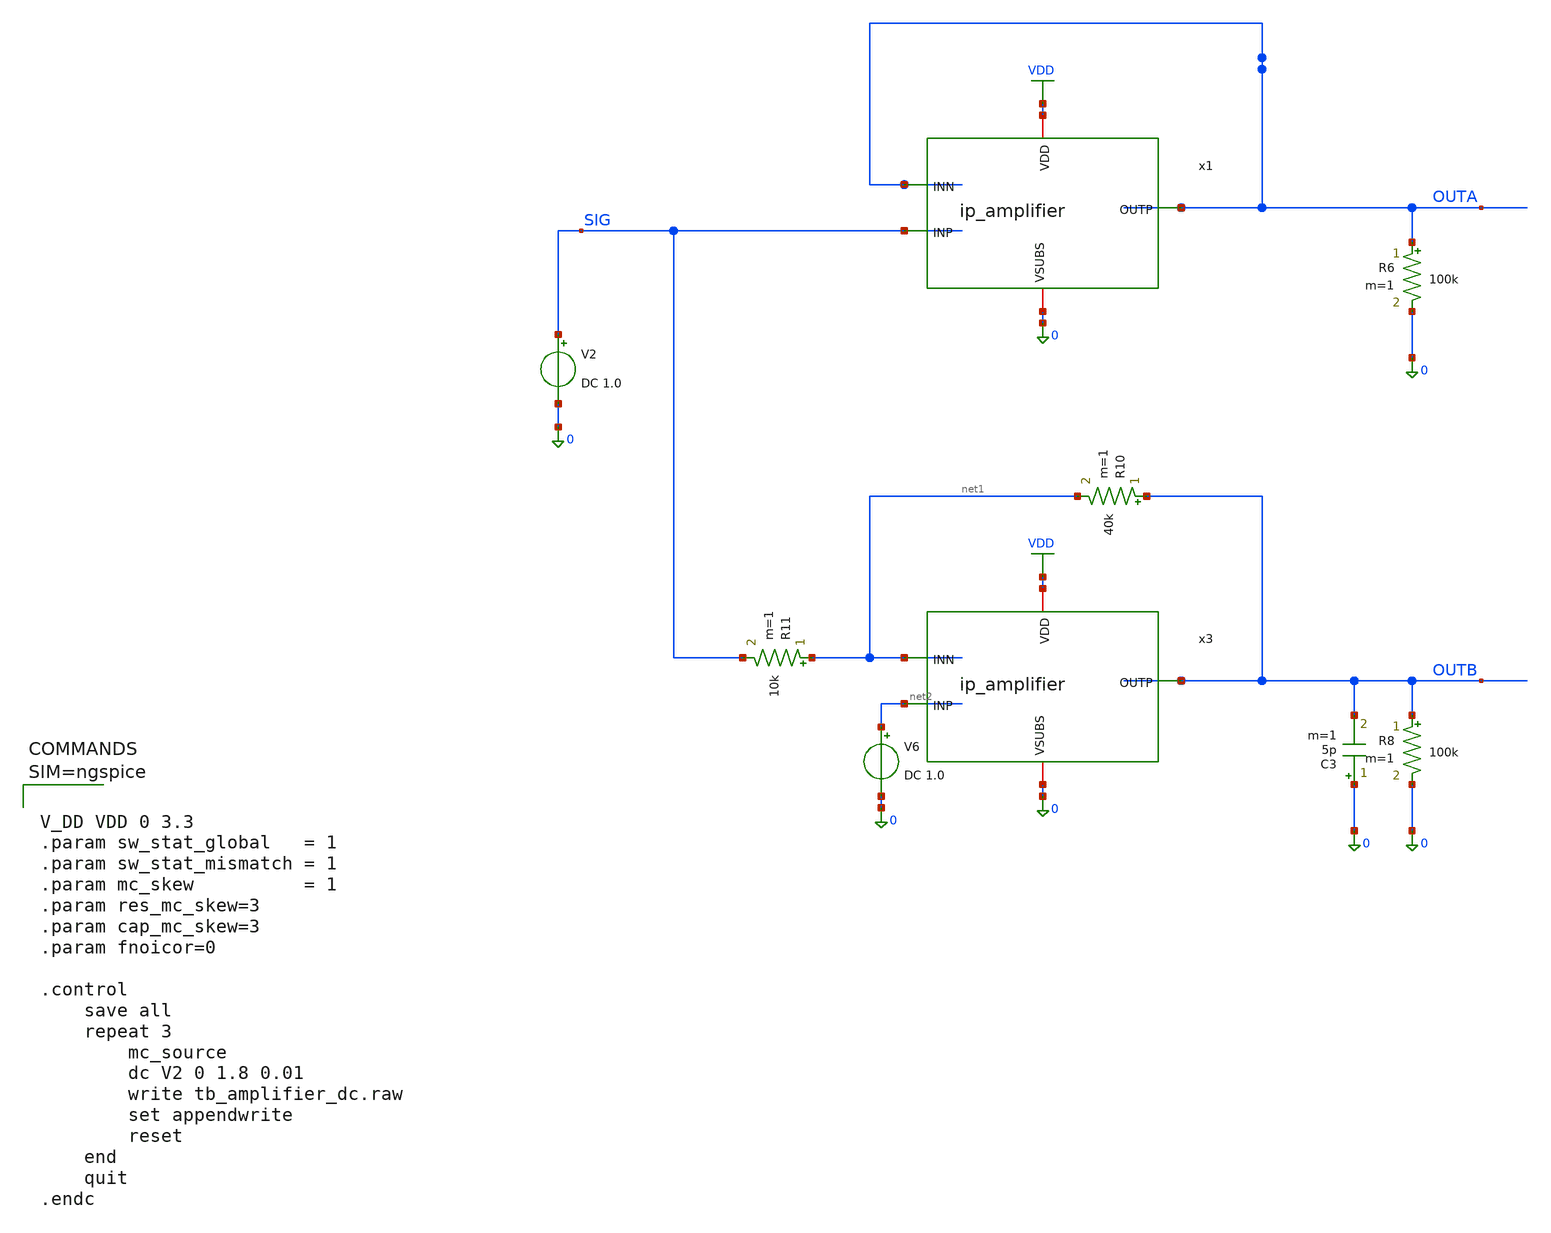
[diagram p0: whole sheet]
** sch_path: xschem/tb_amplifier_dc.sch
**.subckt tb_amplifier_dc
x1 VDD OUTA SIG OUTA 0 ip_amplifier
R6 OUTA 0 100k m=1
x3 VDD OUTB net2 net1 0 ip_amplifier
R8 OUTB 0 100k m=1
R10 OUTB net1 40k m=1
R11 net1 SIG 10k m=1
V6 net2 0 DC 1.0
C3 0 OUTB 5p m=1
V2 SIG 0 DC 1.0
**** begin user architecture code

.lib $::180MCU_MODELS/sm141064.ngspice statistical
.lib $::180MCU_MODELS/sm141064.ngspice moscap_typical
.lib $::180MCU_MODELS/sm141064.ngspice diode_typical
.lib $::180MCU_MODELS/sm141064.ngspice res_statistical




V_DD VDD 0 3.3
.param sw_stat_global   = 1
.param sw_stat_mismatch = 1
.param mc_skew          = 1
.param res_mc_skew=3
.param cap_mc_skew=3
.param fnoicor=0

.control
	save all
	repeat 3
		mc_source
		dc V2 0 1.8 0.01
		write tb_amplifier_dc.raw
		set appendwrite
		reset
	end
	quit
.endc



**** end user architecture code
**.ends

* expanding   symbol:  ip_amplifier.sym # of pins=5
** sym_path: xschem/ip_amplifier.sym
** sch_path: xschem/ip_amplifier.sch
.subckt ip_amplifier VDD OUTP INP INN VSUBS
*.iopin VDD
*.iopin VSUBS
*.ipin INP
*.ipin INN
*.opin OUTP
XM1 net10 INP net8 VDD pfet_06v0 L=0.7u W=7.0u nf=1 ad='int((nf+1)/2) * W/nf * 0.18u' as='int((nf+2)/2) * W/nf * 0.18u'
+ pd='2*int((nf+1)/2) * (W/nf + 0.18u)' ps='2*int((nf+2)/2) * (W/nf + 0.18u)' nrd='0.18u / W' nrs='0.18u / W'
+ sa=0 sb=0 sd=0 m=3 par=3
XM2 net9 INN net8 VDD pfet_06v0 L=0.7u W=7.0u nf=1 ad='int((nf+1)/2) * W/nf * 0.18u' as='int((nf+2)/2) * W/nf * 0.18u'
+ pd='2*int((nf+1)/2) * (W/nf + 0.18u)' ps='2*int((nf+2)/2) * (W/nf + 0.18u)' nrd='0.18u / W' nrs='0.18u / W'
+ sa=0 sb=0 sd=0 m=3 par=3
XM5 net10 net1 VSUBS vsubs nfet_06v0 L=2u W=5u nf=1 ad='int((nf+1)/2) * W/nf * 0.18u' as='int((nf+2)/2) * W/nf * 0.18u'
+ pd='2*int((nf+1)/2) * (W/nf + 0.18u)' ps='2*int((nf+2)/2) * (W/nf + 0.18u)' nrd='0.18u / W' nrs='0.18u / W'
+ sa=0 sb=0 sd=0 m=1 par=1
XM6 net9 net1 VSUBS vsubs nfet_06v0 L=2u W=5u nf=1 ad='int((nf+1)/2) * W/nf * 0.18u' as='int((nf+2)/2) * W/nf * 0.18u'
+ pd='2*int((nf+1)/2) * (W/nf + 0.18u)' ps='2*int((nf+2)/2) * (W/nf + 0.18u)' nrd='0.18u / W' nrs='0.18u / W'
+ sa=0 sb=0 sd=0 m=1 par=1
XM3 net3 net1 VSUBS vsubs nfet_06v0 L=1u W=5u nf=1 ad='int((nf+1)/2) * W/nf * 0.18u' as='int((nf+2)/2) * W/nf * 0.18u'
+ pd='2*int((nf+1)/2) * (W/nf + 0.18u)' ps='2*int((nf+2)/2) * (W/nf + 0.18u)' nrd='0.18u / W' nrs='0.18u / W'
+ sa=0 sb=0 sd=0 m=5 par=5
XM4 net2 net1 VSUBS vsubs nfet_06v0 L=1u W=5u nf=1 ad='int((nf+1)/2) * W/nf * 0.18u' as='int((nf+2)/2) * W/nf * 0.18u'
+ pd='2*int((nf+1)/2) * (W/nf + 0.18u)' ps='2*int((nf+2)/2) * (W/nf + 0.18u)' nrd='0.18u / W' nrs='0.18u / W'
+ sa=0 sb=0 sd=0 m=1 par=1
XM7 net1 net1 net3 vsubs nfet_06v0 L=0.7u W=5u nf=1 ad='int((nf+1)/2) * W/nf * 0.18u' as='int((nf+2)/2) * W/nf * 0.18u'
+ pd='2*int((nf+1)/2) * (W/nf + 0.18u)' ps='2*int((nf+2)/2) * (W/nf + 0.18u)' nrd='0.18u / W' nrs='0.18u / W'
+ sa=0 sb=0 sd=0 m=7 par=7
XM8 net4 net1 net2 vsubs nfet_06v0 L=0.7u W=5u nf=1 ad='int((nf+1)/2) * W/nf * 0.18u' as='int((nf+2)/2) * W/nf * 0.18u'
+ pd='2*int((nf+1)/2) * (W/nf + 0.18u)' ps='2*int((nf+2)/2) * (W/nf + 0.18u)' nrd='0.18u / W' nrs='0.18u / W'
+ sa=0 sb=0 sd=0 m=7 par=7
XM9 net5 net7 VDD VDD pfet_06v0 L=1u W=6u nf=1 ad='int((nf+1)/2) * W/nf * 0.18u' as='int((nf+2)/2) * W/nf * 0.18u'
+ pd='2*int((nf+1)/2) * (W/nf + 0.18u)' ps='2*int((nf+2)/2) * (W/nf + 0.18u)' nrd='0.18u / W' nrs='0.18u / W'
+ sa=0 sb=0 sd=0 m=1 par=1
XM10 net6 net7 VDD VDD pfet_06v0 L=1u W=6u nf=1 ad='int((nf+1)/2) * W/nf * 0.18u' as='int((nf+2)/2) * W/nf * 0.18u'
+ pd='2*int((nf+1)/2) * (W/nf + 0.18u)' ps='2*int((nf+2)/2) * (W/nf + 0.18u)' nrd='0.18u / W' nrs='0.18u / W'
+ sa=0 sb=0 sd=0 m=1 par=1
XM11 net7 net7 net5 VDD pfet_06v0 L=0.7u W=7u nf=1 ad='int((nf+1)/2) * W/nf * 0.18u' as='int((nf+2)/2) * W/nf * 0.18u'
+ pd='2*int((nf+1)/2) * (W/nf + 0.18u)' ps='2*int((nf+2)/2) * (W/nf + 0.18u)' nrd='0.18u / W' nrs='0.18u / W'
+ sa=0 sb=0 sd=0 m=5 par=5
XM12 net8 net7 net6 VDD pfet_06v0 L=0.7u W=7u nf=1 ad='int((nf+1)/2) * W/nf * 0.18u' as='int((nf+2)/2) * W/nf * 0.18u'
+ pd='2*int((nf+1)/2) * (W/nf + 0.18u)' ps='2*int((nf+2)/2) * (W/nf + 0.18u)' nrd='0.18u / W' nrs='0.18u / W'
+ sa=0 sb=0 sd=0 m=5 par=5
XM13 net11 net1 net9 vsubs nfet_06v0 L=0.7u W=7u nf=1 ad='int((nf+1)/2) * W/nf * 0.18u' as='int((nf+2)/2) * W/nf * 0.18u'
+ pd='2*int((nf+1)/2) * (W/nf + 0.18u)' ps='2*int((nf+2)/2) * (W/nf + 0.18u)' nrd='0.18u / W' nrs='0.18u / W'
+ sa=0 sb=0 sd=0 m=1 par=1
XM14 COMP net1 net10 vsubs nfet_06v0 L=0.7u W=7u nf=1 ad='int((nf+1)/2) * W/nf * 0.18u' as='int((nf+2)/2) * W/nf * 0.18u'
+ pd='2*int((nf+1)/2) * (W/nf + 0.18u)' ps='2*int((nf+2)/2) * (W/nf + 0.18u)' nrd='0.18u / W' nrs='0.18u / W'
+ sa=0 sb=0 sd=0 m=1 par=1
XM15 net11 net11 VDD VDD pfet_06v0 L=0.7u W=7u nf=1 ad='int((nf+1)/2) * W/nf * 0.18u' as='int((nf+2)/2) * W/nf * 0.18u'
+ pd='2*int((nf+1)/2) * (W/nf + 0.18u)' ps='2*int((nf+2)/2) * (W/nf + 0.18u)' nrd='0.18u / W' nrs='0.18u / W'
+ sa=0 sb=0 sd=0 m=1 par=1
XM16 COMP net11 VDD VDD pfet_06v0 L=0.7u W=7u nf=1 ad='int((nf+1)/2) * W/nf * 0.18u' as='int((nf+2)/2) * W/nf * 0.18u'
+ pd='2*int((nf+1)/2) * (W/nf + 0.18u)' ps='2*int((nf+2)/2) * (W/nf + 0.18u)' nrd='0.18u / W' nrs='0.18u / W'
+ sa=0 sb=0 sd=0 m=1 par=1
XM17 OUTP COMP VDD VDD pfet_06v0 L=0.5u W=5u nf=1 ad='int((nf+1)/2) * W/nf * 0.18u' as='int((nf+2)/2) * W/nf * 0.18u'
+ pd='2*int((nf+1)/2) * (W/nf + 0.18u)' ps='2*int((nf+2)/2) * (W/nf + 0.18u)' nrd='0.18u / W' nrs='0.18u / W'
+ sa=0 sb=0 sd=0 m=12 par=12
XM18 OUTP net10 VSUBS vsubs nfet_06v0 L=0.7u W=5u nf=1 ad='int((nf+1)/2) * W/nf * 0.18u' as='int((nf+2)/2) * W/nf * 0.18u'
+ pd='2*int((nf+1)/2) * (W/nf + 0.18u)' ps='2*int((nf+2)/2) * (W/nf + 0.18u)' nrd='0.18u / W' nrs='0.18u / W'
+ sa=0 sb=0 sd=0 m=6 par=6
XR3 net1 net14 vsubs ppolyf_u_1k_6p0 r_width=1e-6 r_length=6e-6 m=1
XR6 net14 net13 vsubs ppolyf_u_1k_6p0 r_width=1e-6 r_length=6e-6 m=1
XR7 net13 net12 vsubs ppolyf_u_1k_6p0 r_width=1e-6 r_length=6e-6 m=1
XR8 net12 net15 vsubs ppolyf_u_1k_6p0 r_width=1e-6 r_length=4e-6 m=1
Vmeas VDD net15 0
Vmeas1 net7 net4 0
XC1 OUTP net16 cap_nmos_03v3 c_width=12e-6 c_length=18e-6 m=1
XC2 COMP net19 cap_nmos_03v3 c_width=12e-6 c_length=18e-6 m=1
XR12 net16 net17 vsubs ppolyf_u_1k_6p0 r_width=1e-6 r_length=5e-6 m=1
XR13 net17 COMP vsubs ppolyf_u_1k_6p0 r_width=1e-6 r_length=5e-6 m=1
XR15 OUTP net18 vsubs ppolyf_u_1k_6p0 r_width=1e-6 r_length=5e-6 m=1
XR16 net18 net19 vsubs ppolyf_u_1k_6p0 r_width=1e-6 r_length=5e-6 m=1
.ends

.GLOBAL VDD
.end
